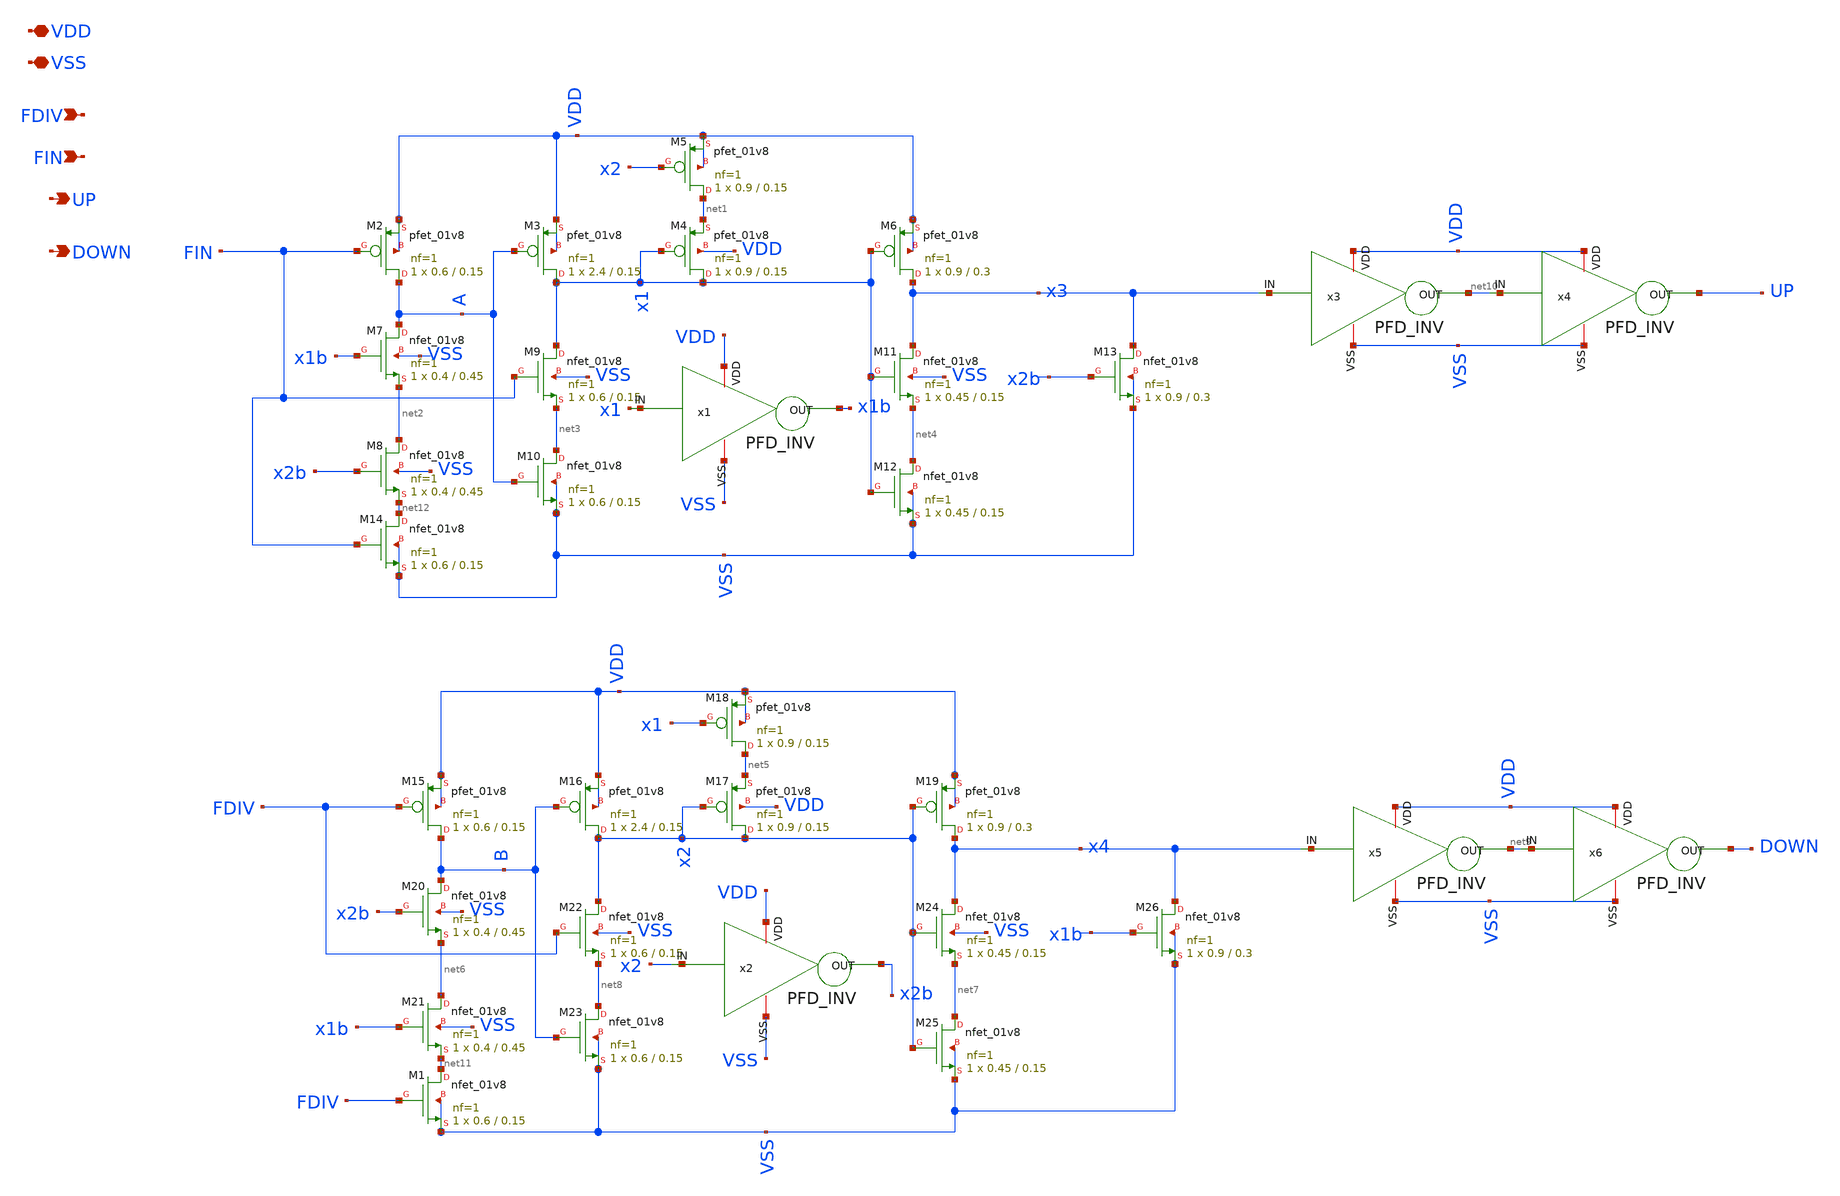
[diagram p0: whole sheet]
** sch_path: Xschem/PLL_TOP/PFD.sch
**.subckt PFD FDIV FIN UP DOWN VSS VDD
*.ipin FDIV
*.ipin FIN
*.opin UP
*.opin DOWN
*.iopin VSS
*.iopin VDD
XM2 A FIN VDD VDD sky130_fd_pr__pfet_01v8 L=0.15 W=0.6 nf=1 ad='int((nf+1)/2) * W/nf * 0.29' as='int((nf+2)/2) * W/nf * 0.29'
+ pd='2*int((nf+1)/2) * (W/nf + 0.29)' ps='2*int((nf+2)/2) * (W/nf + 0.29)' nrd='0.29 / W' nrs='0.29 / W'
+ sa=0 sb=0 sd=0 mult=1 m=1
XM3 x1 A VDD VDD sky130_fd_pr__pfet_01v8 L=0.15 W=2.4 nf=1 ad='int((nf+1)/2) * W/nf * 0.29' as='int((nf+2)/2) * W/nf * 0.29'
+ pd='2*int((nf+1)/2) * (W/nf + 0.29)' ps='2*int((nf+2)/2) * (W/nf + 0.29)' nrd='0.29 / W' nrs='0.29 / W'
+ sa=0 sb=0 sd=0 mult=1 m=1
XM4 x1 x1 net1 VDD sky130_fd_pr__pfet_01v8 L=0.15 W=0.9 nf=1 ad='int((nf+1)/2) * W/nf * 0.29' as='int((nf+2)/2) * W/nf * 0.29'
+ pd='2*int((nf+1)/2) * (W/nf + 0.29)' ps='2*int((nf+2)/2) * (W/nf + 0.29)' nrd='0.29 / W' nrs='0.29 / W'
+ sa=0 sb=0 sd=0 mult=1 m=1
XM5 net1 x2 VDD VDD sky130_fd_pr__pfet_01v8 L=0.15 W=0.9 nf=1 ad='int((nf+1)/2) * W/nf * 0.29' as='int((nf+2)/2) * W/nf * 0.29'
+ pd='2*int((nf+1)/2) * (W/nf + 0.29)' ps='2*int((nf+2)/2) * (W/nf + 0.29)' nrd='0.29 / W' nrs='0.29 / W'
+ sa=0 sb=0 sd=0 mult=1 m=1
XM6 x3 x1 VDD VDD sky130_fd_pr__pfet_01v8 L=0.3 W=0.9 nf=1 ad='int((nf+1)/2) * W/nf * 0.29' as='int((nf+2)/2) * W/nf * 0.29'
+ pd='2*int((nf+1)/2) * (W/nf + 0.29)' ps='2*int((nf+2)/2) * (W/nf + 0.29)' nrd='0.29 / W' nrs='0.29 / W'
+ sa=0 sb=0 sd=0 mult=1 m=1
XM7 A x1b net2 VSS sky130_fd_pr__nfet_01v8 L=0.45 W=0.4 nf=1 ad='int((nf+1)/2) * W/nf * 0.29' as='int((nf+2)/2) * W/nf * 0.29'
+ pd='2*int((nf+1)/2) * (W/nf + 0.29)' ps='2*int((nf+2)/2) * (W/nf + 0.29)' nrd='0.29 / W' nrs='0.29 / W'
+ sa=0 sb=0 sd=0 mult=1 m=1
XM8 net2 x2b net12 VSS sky130_fd_pr__nfet_01v8 L=0.45 W=0.4 nf=1 ad='int((nf+1)/2) * W/nf * 0.29' as='int((nf+2)/2) * W/nf * 0.29'
+ pd='2*int((nf+1)/2) * (W/nf + 0.29)' ps='2*int((nf+2)/2) * (W/nf + 0.29)' nrd='0.29 / W' nrs='0.29 / W'
+ sa=0 sb=0 sd=0 mult=1 m=1
XM9 x1 FIN net3 VSS sky130_fd_pr__nfet_01v8 L=0.15 W=0.6 nf=1 ad='int((nf+1)/2) * W/nf * 0.29' as='int((nf+2)/2) * W/nf * 0.29'
+ pd='2*int((nf+1)/2) * (W/nf + 0.29)' ps='2*int((nf+2)/2) * (W/nf + 0.29)' nrd='0.29 / W' nrs='0.29 / W'
+ sa=0 sb=0 sd=0 mult=1 m=1
XM10 net3 A VSS VSS sky130_fd_pr__nfet_01v8 L=0.15 W=0.6 nf=1 ad='int((nf+1)/2) * W/nf * 0.29' as='int((nf+2)/2) * W/nf * 0.29'
+ pd='2*int((nf+1)/2) * (W/nf + 0.29)' ps='2*int((nf+2)/2) * (W/nf + 0.29)' nrd='0.29 / W' nrs='0.29 / W'
+ sa=0 sb=0 sd=0 mult=1 m=1
XM11 x3 x1 net4 VSS sky130_fd_pr__nfet_01v8 L=0.15 W=0.45 nf=1 ad='int((nf+1)/2) * W/nf * 0.29' as='int((nf+2)/2) * W/nf * 0.29'
+ pd='2*int((nf+1)/2) * (W/nf + 0.29)' ps='2*int((nf+2)/2) * (W/nf + 0.29)' nrd='0.29 / W' nrs='0.29 / W'
+ sa=0 sb=0 sd=0 mult=1 m=1
XM12 net4 x1 VSS VSS sky130_fd_pr__nfet_01v8 L=0.15 W=0.45 nf=1 ad='int((nf+1)/2) * W/nf * 0.29' as='int((nf+2)/2) * W/nf * 0.29'
+ pd='2*int((nf+1)/2) * (W/nf + 0.29)' ps='2*int((nf+2)/2) * (W/nf + 0.29)' nrd='0.29 / W' nrs='0.29 / W'
+ sa=0 sb=0 sd=0 mult=1 m=1
XM13 x3 x2b VSS VSS sky130_fd_pr__nfet_01v8 L=0.3 W=0.9 nf=1 ad='int((nf+1)/2) * W/nf * 0.29' as='int((nf+2)/2) * W/nf * 0.29'
+ pd='2*int((nf+1)/2) * (W/nf + 0.29)' ps='2*int((nf+2)/2) * (W/nf + 0.29)' nrd='0.29 / W' nrs='0.29 / W'
+ sa=0 sb=0 sd=0 mult=1 m=1
XM15 B FDIV VDD VDD sky130_fd_pr__pfet_01v8 L=0.15 W=0.6 nf=1 ad='int((nf+1)/2) * W/nf * 0.29' as='int((nf+2)/2) * W/nf * 0.29'
+ pd='2*int((nf+1)/2) * (W/nf + 0.29)' ps='2*int((nf+2)/2) * (W/nf + 0.29)' nrd='0.29 / W' nrs='0.29 / W'
+ sa=0 sb=0 sd=0 mult=1 m=1
XM16 x2 B VDD VDD sky130_fd_pr__pfet_01v8 L=0.15 W=2.4 nf=1 ad='int((nf+1)/2) * W/nf * 0.29' as='int((nf+2)/2) * W/nf * 0.29'
+ pd='2*int((nf+1)/2) * (W/nf + 0.29)' ps='2*int((nf+2)/2) * (W/nf + 0.29)' nrd='0.29 / W' nrs='0.29 / W'
+ sa=0 sb=0 sd=0 mult=1 m=1
XM17 x2 x2 net5 VDD sky130_fd_pr__pfet_01v8 L=0.15 W=0.9 nf=1 ad='int((nf+1)/2) * W/nf * 0.29' as='int((nf+2)/2) * W/nf * 0.29'
+ pd='2*int((nf+1)/2) * (W/nf + 0.29)' ps='2*int((nf+2)/2) * (W/nf + 0.29)' nrd='0.29 / W' nrs='0.29 / W'
+ sa=0 sb=0 sd=0 mult=1 m=1
XM18 net5 x1 VDD VDD sky130_fd_pr__pfet_01v8 L=0.15 W=0.9 nf=1 ad='int((nf+1)/2) * W/nf * 0.29' as='int((nf+2)/2) * W/nf * 0.29'
+ pd='2*int((nf+1)/2) * (W/nf + 0.29)' ps='2*int((nf+2)/2) * (W/nf + 0.29)' nrd='0.29 / W' nrs='0.29 / W'
+ sa=0 sb=0 sd=0 mult=1 m=1
XM19 x4 x2 VDD VDD sky130_fd_pr__pfet_01v8 L=0.3 W=0.9 nf=1 ad='int((nf+1)/2) * W/nf * 0.29' as='int((nf+2)/2) * W/nf * 0.29'
+ pd='2*int((nf+1)/2) * (W/nf + 0.29)' ps='2*int((nf+2)/2) * (W/nf + 0.29)' nrd='0.29 / W' nrs='0.29 / W'
+ sa=0 sb=0 sd=0 mult=1 m=1
XM20 B x2b net6 VSS sky130_fd_pr__nfet_01v8 L=0.45 W=0.4 nf=1 ad='int((nf+1)/2) * W/nf * 0.29' as='int((nf+2)/2) * W/nf * 0.29'
+ pd='2*int((nf+1)/2) * (W/nf + 0.29)' ps='2*int((nf+2)/2) * (W/nf + 0.29)' nrd='0.29 / W' nrs='0.29 / W'
+ sa=0 sb=0 sd=0 mult=1 m=1
XM21 net6 x1b net11 VSS sky130_fd_pr__nfet_01v8 L=0.45 W=0.4 nf=1 ad='int((nf+1)/2) * W/nf * 0.29' as='int((nf+2)/2) * W/nf * 0.29'
+ pd='2*int((nf+1)/2) * (W/nf + 0.29)' ps='2*int((nf+2)/2) * (W/nf + 0.29)' nrd='0.29 / W' nrs='0.29 / W'
+ sa=0 sb=0 sd=0 mult=1 m=1
XM22 x2 FDIV net8 VSS sky130_fd_pr__nfet_01v8 L=0.15 W=0.6 nf=1 ad='int((nf+1)/2) * W/nf * 0.29' as='int((nf+2)/2) * W/nf * 0.29'
+ pd='2*int((nf+1)/2) * (W/nf + 0.29)' ps='2*int((nf+2)/2) * (W/nf + 0.29)' nrd='0.29 / W' nrs='0.29 / W'
+ sa=0 sb=0 sd=0 mult=1 m=1
XM23 net8 B VSS VSS sky130_fd_pr__nfet_01v8 L=0.15 W=0.6 nf=1 ad='int((nf+1)/2) * W/nf * 0.29' as='int((nf+2)/2) * W/nf * 0.29'
+ pd='2*int((nf+1)/2) * (W/nf + 0.29)' ps='2*int((nf+2)/2) * (W/nf + 0.29)' nrd='0.29 / W' nrs='0.29 / W'
+ sa=0 sb=0 sd=0 mult=1 m=1
XM24 x4 x2 net7 VSS sky130_fd_pr__nfet_01v8 L=0.15 W=0.45 nf=1 ad='int((nf+1)/2) * W/nf * 0.29' as='int((nf+2)/2) * W/nf * 0.29'
+ pd='2*int((nf+1)/2) * (W/nf + 0.29)' ps='2*int((nf+2)/2) * (W/nf + 0.29)' nrd='0.29 / W' nrs='0.29 / W'
+ sa=0 sb=0 sd=0 mult=1 m=1
XM25 net7 x2 VSS VSS sky130_fd_pr__nfet_01v8 L=0.15 W=0.45 nf=1 ad='int((nf+1)/2) * W/nf * 0.29' as='int((nf+2)/2) * W/nf * 0.29'
+ pd='2*int((nf+1)/2) * (W/nf + 0.29)' ps='2*int((nf+2)/2) * (W/nf + 0.29)' nrd='0.29 / W' nrs='0.29 / W'
+ sa=0 sb=0 sd=0 mult=1 m=1
XM26 x4 x1b VSS VSS sky130_fd_pr__nfet_01v8 L=0.3 W=0.9 nf=1 ad='int((nf+1)/2) * W/nf * 0.29' as='int((nf+2)/2) * W/nf * 0.29'
+ pd='2*int((nf+1)/2) * (W/nf + 0.29)' ps='2*int((nf+2)/2) * (W/nf + 0.29)' nrd='0.29 / W' nrs='0.29 / W'
+ sa=0 sb=0 sd=0 mult=1 m=1
XM1 net11 FDIV VSS VSS sky130_fd_pr__nfet_01v8 L=0.15 W=0.6 nf=1 ad='int((nf+1)/2) * W/nf * 0.29' as='int((nf+2)/2) * W/nf * 0.29'
+ pd='2*int((nf+1)/2) * (W/nf + 0.29)' ps='2*int((nf+2)/2) * (W/nf + 0.29)' nrd='0.29 / W' nrs='0.29 / W'
+ sa=0 sb=0 sd=0 mult=1 m=1
XM14 net12 FIN VSS VSS sky130_fd_pr__nfet_01v8 L=0.15 W=0.6 nf=1 ad='int((nf+1)/2) * W/nf * 0.29' as='int((nf+2)/2) * W/nf * 0.29'
+ pd='2*int((nf+1)/2) * (W/nf + 0.29)' ps='2*int((nf+2)/2) * (W/nf + 0.29)' nrd='0.29 / W' nrs='0.29 / W'
+ sa=0 sb=0 sd=0 mult=1 m=1
x1 VDD VSS x1 x1b PFD_INV
x2 VDD VSS x2 x2b PFD_INV
x3 VDD VSS x3 net10 PFD_INV
x4 VDD VSS net10 UP PFD_INV
x5 VDD VSS x4 net9 PFD_INV
x6 VDD VSS net9 DOWN PFD_INV
**.ends

* expanding   symbol:  /home/shahid/Sky130Projects/TOP/PFD_INV.sym # of pins=4
** sym_path: /home/shahid/Sky130Projects/TOP/PFD_INV.sym
** sch_path: /home/shahid/Sky130Projects/TOP/PFD_INV.sch
.subckt PFD_INV VDD VSS IN OUT
*.iopin VDD
*.iopin VSS
*.ipin IN
*.opin OUT
XM1 OUT IN VDD VDD sky130_fd_pr__pfet_01v8 L=0.15 W=0.8 nf=1 ad='int((nf+1)/2) * W/nf * 0.29' as='int((nf+2)/2) * W/nf * 0.29'
+ pd='2*int((nf+1)/2) * (W/nf + 0.29)' ps='2*int((nf+2)/2) * (W/nf + 0.29)' nrd='0.29 / W' nrs='0.29 / W'
+ sa=0 sb=0 sd=0 mult=1 m=1
XM3 OUT IN VSS VSS sky130_fd_pr__nfet_01v8 L=0.15 W=0.4 nf=1 ad='int((nf+1)/2) * W/nf * 0.29' as='int((nf+2)/2) * W/nf * 0.29'
+ pd='2*int((nf+1)/2) * (W/nf + 0.29)' ps='2*int((nf+2)/2) * (W/nf + 0.29)' nrd='0.29 / W' nrs='0.29 / W'
+ sa=0 sb=0 sd=0 mult=1 m=1
.ends

.end
